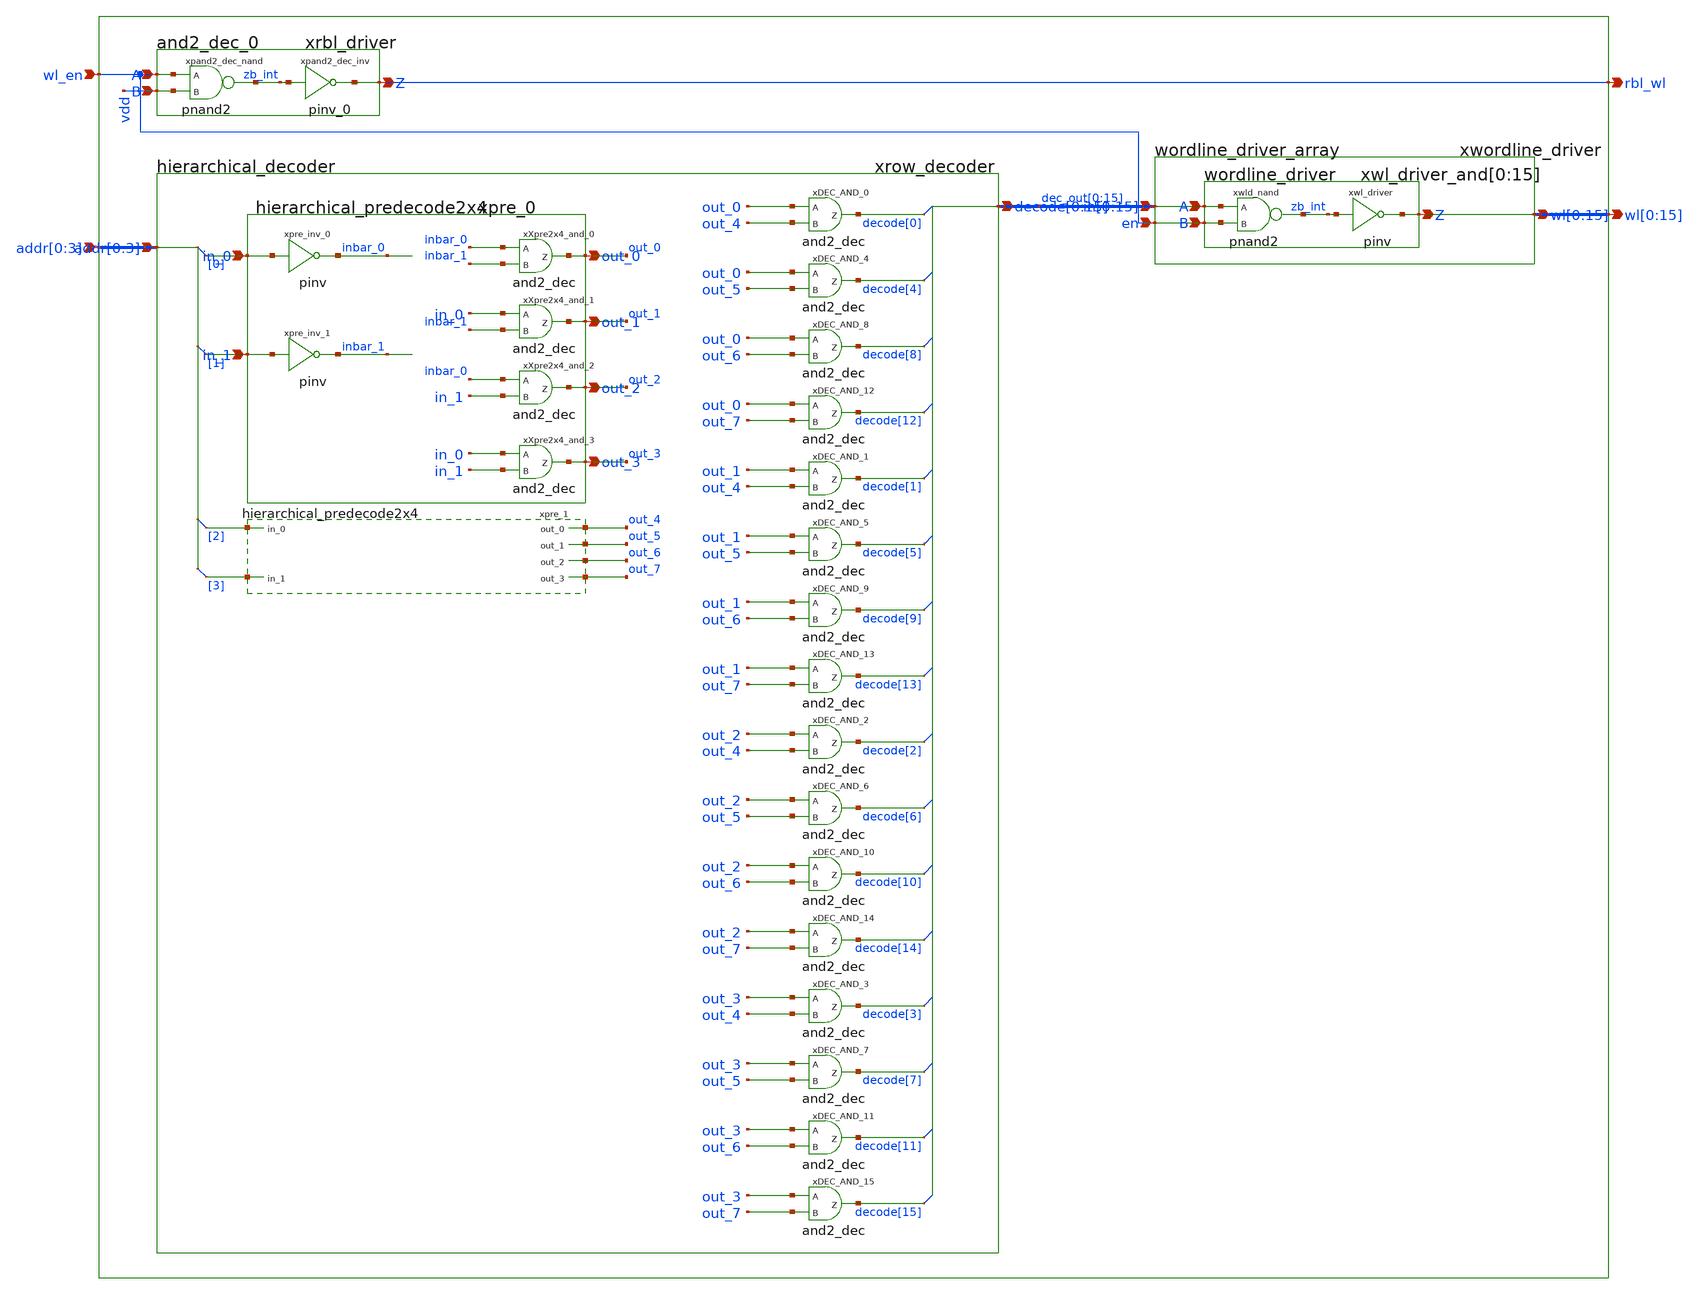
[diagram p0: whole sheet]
** sch_path: sram_2_64_scn4m_lcc/port_address.sch
**.subckt port_address addr[0],addr[1],addr[2],addr[3] wl_en
*+ wl[0],wl[1],wl[2],wl[3],wl[4],wl[5],wl[6],wl[7],wl[8],wl[9],wl[10],wl[11],wl[12],wl[13],wl[14],wl[15] rbl_wl
*.ipin addr[0],addr[1],addr[2],addr[3]
*.ipin wl_en
*.opin
*+ wl[0],wl[1],wl[2],wl[3],wl[4],wl[5],wl[6],wl[7],wl[8],wl[9],wl[10],wl[11],wl[12],wl[13],wl[14],wl[15]
*.opin rbl_wl
xrow_decoder addr[0] addr[1] addr[2] addr[3] dec_out[0] dec_out[1] dec_out[2] dec_out[3] dec_out[4]
+ dec_out[5] dec_out[6] dec_out[7] dec_out[8] dec_out[9] dec_out[10] dec_out[11] dec_out[12] dec_out[13]
+ dec_out[14] dec_out[15] vdd gnd hierarchical_decoder
xwordline_driver dec_out[0] dec_out[1] dec_out[2] dec_out[3] dec_out[4] dec_out[5] dec_out[6]
+ dec_out[7] dec_out[8] dec_out[9] dec_out[10] dec_out[11] dec_out[12] dec_out[13] dec_out[14] dec_out[15] wl[0]
+ wl[1] wl[2] wl[3] wl[4] wl[5] wl[6] wl[7] wl[8] wl[9] wl[10] wl[11] wl[12] wl[13] wl[14] wl[15] wl_en vdd
+ gnd wordline_driver_array
xrbl_driver wl_en vdd rbl_wl vdd gnd and2_dec_0
**.ends
.end
